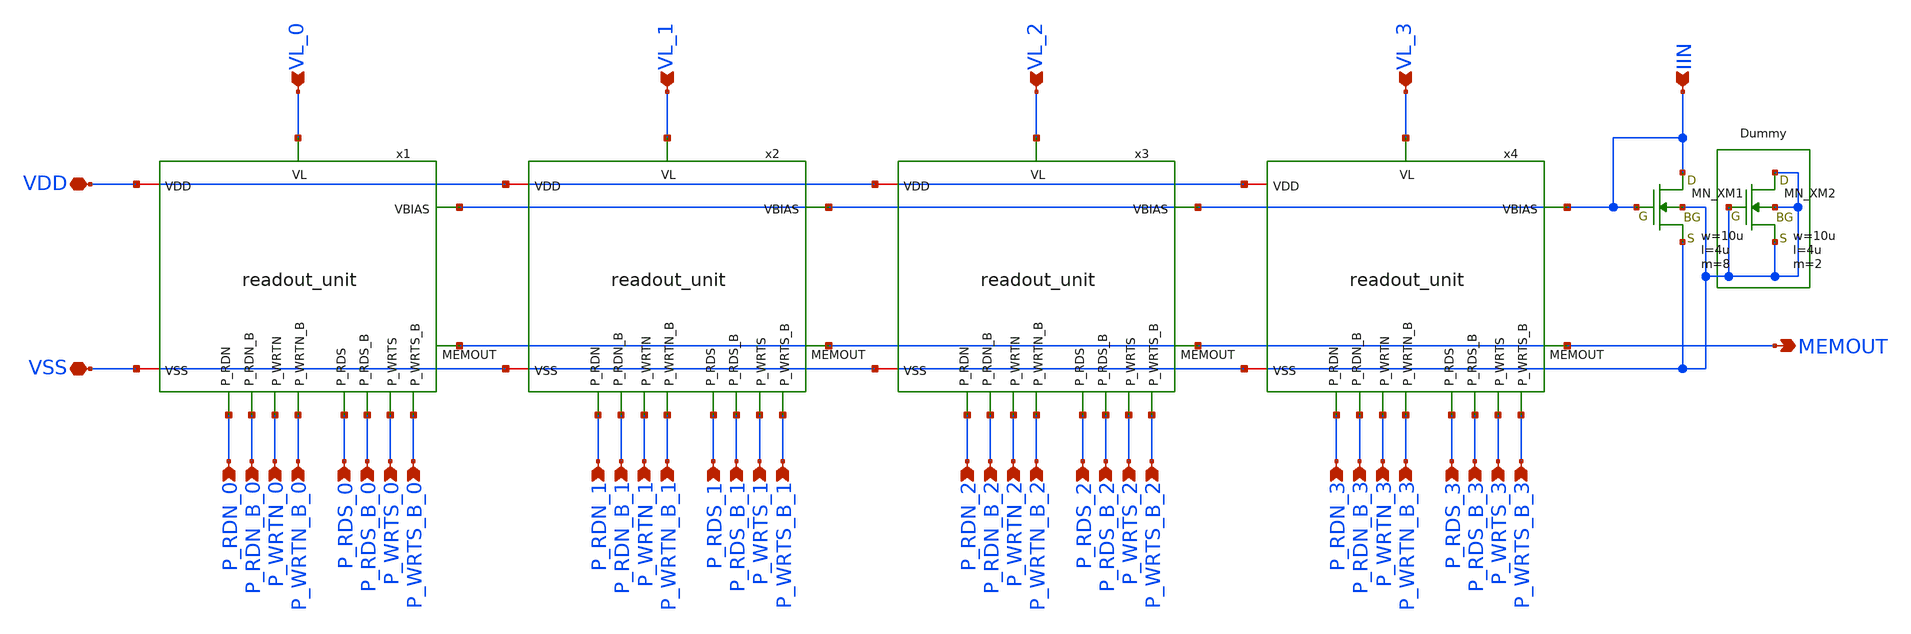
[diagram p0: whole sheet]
** sch_path: member_project/imager/YuMaehashi/design/readout.sch
**.subckt readout VL_0 VDD VSS IIN MEMOUT P_RDN_0 P_RDN_B_0 P_WRTN_0 P_WRTN_B_0 P_RDS_0 P_RDS_B_0
*+ P_WRTS_0 P_WRTS_B_0 VL_1 VL_2 VL_3 P_RDN_1 P_RDN_B_1 P_WRTN_1 P_WRTN_B_1 P_RDS_1 P_RDS_B_1 P_WRTS_1
*+ P_WRTS_B_1 P_RDN_2 P_RDN_B_2 P_WRTN_2 P_WRTN_B_2 P_RDS_2 P_RDS_B_2 P_WRTS_2 P_WRTS_B_2 P_RDN_3 P_RDN_B_3
*+ P_WRTN_3 P_WRTN_B_3 P_RDS_3 P_RDS_B_3 P_WRTS_3 P_WRTS_B_3
*.ipin VL_0
*.iopin VDD
*.iopin VSS
*.ipin IIN
*.opin MEMOUT
*.ipin P_RDN_0
*.ipin P_RDN_B_0
*.ipin P_WRTN_0
*.ipin P_WRTN_B_0
*.ipin P_RDS_0
*.ipin P_RDS_B_0
*.ipin P_WRTS_0
*.ipin P_WRTS_B_0
*.ipin VL_1
*.ipin VL_2
*.ipin VL_3
*.ipin P_RDN_1
*.ipin P_RDN_B_1
*.ipin P_WRTN_1
*.ipin P_WRTN_B_1
*.ipin P_RDS_1
*.ipin P_RDS_B_1
*.ipin P_WRTS_1
*.ipin P_WRTS_B_1
*.ipin P_RDN_2
*.ipin P_RDN_B_2
*.ipin P_WRTN_2
*.ipin P_WRTN_B_2
*.ipin P_RDS_2
*.ipin P_RDS_B_2
*.ipin P_WRTS_2
*.ipin P_WRTS_B_2
*.ipin P_RDN_3
*.ipin P_RDN_B_3
*.ipin P_WRTN_3
*.ipin P_WRTN_B_3
*.ipin P_RDS_3
*.ipin P_RDS_B_3
*.ipin P_WRTS_3
*.ipin P_WRTS_B_3
x1 VL_0 VDD IIN VSS P_WRTN_0 P_WRTN_B_0 P_WRTS_0 P_WRTS_B_0 MEMOUT P_RDS_B_0 P_RDS_0 P_RDN_B_0
+ P_RDN_0 readout_unit
x2 VL_1 VDD IIN VSS P_WRTN_1 P_WRTN_B_1 P_WRTS_1 P_WRTS_B_1 MEMOUT P_RDS_B_1 P_RDS_1 P_RDN_B_1
+ P_RDN_1 readout_unit
x3 VL_2 VDD IIN VSS P_WRTN_2 P_WRTN_B_2 P_WRTS_2 P_WRTS_B_2 MEMOUT P_RDS_B_2 P_RDS_2 P_RDN_B_2
+ P_RDN_2 readout_unit
x4 VL_3 VDD IIN VSS P_WRTN_3 P_WRTN_B_3 P_WRTS_3 P_WRTS_B_3 MEMOUT P_RDS_B_3 P_RDS_3 P_RDN_B_3
+ P_RDN_3 readout_unit
XXM1 IIN IIN VSS VSS NMOS w=10u l=4u nrd=0 nrs=0 m=8
XXM2 VSS VSS VSS VSS NMOS w=10u l=4u nrd=0 nrs=0 m=2
**.ends

* expanding   symbol:  2026_imager/readout_unit.sym # of pins=13
** sym_path: member_project/imager/YuMaehashi/design/readout_unit.sym
** sch_path: member_project/imager/YuMaehashi/design/readout_unit.sch
.subckt readout_unit VL VDD VBIAS VSS P_WRTN P_WRTN_B P_WRTS P_WRTS_B MEMOUT P_RDS_B P_RDS P_RDN_B
+ P_RDN
*.ipin VL
*.iopin VSS
*.ipin VBIAS
*.opin MEMOUT
*.ipin P_RDN
*.ipin P_RDN_B
*.ipin P_WRTN
*.ipin P_WRTN_B
*.ipin P_RDS
*.ipin P_RDS_B
*.ipin P_WRTS
*.ipin P_WRTS_B
*.iopin VDD
XXM1 VL VBIAS VSS VSS NMOS w=10u l=4u nrd=0 nrs=0 m=2
XXC1 MEM_N VSS VSS F_CSIO c=1.017p x=59.5u y=28.5u m=14
XXC2 MEM_S VSS VSS F_CSIO c=1.017p x=59.5u y=28.5u m=14
XXM2 MEM_S P_WRTS_B MEM_S VSS NMOS w=3.4u l=1u nrd=0 nrs=0 m=1
XXM3 MEM_S P_WRTS MEM_S VDD PMOS w=3.4u l=1u nrd=0 nrs=0 m=1
XXM4 VL P_WRTS MEM_S VSS NMOS w=6.8u l=1u nrd=0 nrs=0 m=1
XXM5 VL P_WRTS_B MEM_S VDD PMOS w=6.8u l=1u nrd=0 nrs=0 m=1
XXM6 MEM_N P_WRTN_B MEM_N VSS NMOS w=3.4u l=1u nrd=0 nrs=0 m=1
XXM7 MEM_N P_WRTN MEM_N VDD PMOS w=3.4u l=1u nrd=0 nrs=0 m=1
XXM8 VL P_WRTN MEM_N VSS NMOS w=6.8u l=1u nrd=0 nrs=0 m=1
XXM9 VL P_WRTN_B MEM_N VDD PMOS w=6.8u l=1u nrd=0 nrs=0 m=1
XXM10 MEM_S P_RDS_B MEM_S VSS NMOS w=3.4u l=1u nrd=0 nrs=0 m=1
XXM11 MEM_S P_RDS MEM_S VDD PMOS w=3.4u l=1u nrd=0 nrs=0 m=1
XXM12 MEM_N P_RDN_B MEM_N VSS NMOS w=3.4u l=1u nrd=0 nrs=0 m=1
XXM13 MEM_N P_RDN MEM_N VDD PMOS w=3.4u l=1u nrd=0 nrs=0 m=1
XXM14 MEM_S P_RDS MEMOUT VSS NMOS w=6.8u l=1u nrd=0 nrs=0 m=1
XXM15 MEM_S P_RDS_B MEMOUT VDD PMOS w=6.8u l=1u nrd=0 nrs=0 m=1
XXM16 MEM_N P_RDN MEMOUT VSS NMOS w=6.8u l=1u nrd=0 nrs=0 m=1
XXM17 MEM_N P_RDN_B MEMOUT VDD PMOS w=6.8u l=1u nrd=0 nrs=0 m=1
XXM18 MEMOUT P_RDS_B MEMOUT VSS NMOS w=3.4u l=1u nrd=0 nrs=0 m=1
XXM19 MEMOUT P_RDS MEMOUT VDD PMOS w=3.4u l=1u nrd=0 nrs=0 m=1
XXM20 MEMOUT P_RDN_B MEMOUT VSS NMOS w=3.4u l=1u nrd=0 nrs=0 m=1
XXM21 MEMOUT P_RDN MEMOUT VDD PMOS w=3.4u l=1u nrd=0 nrs=0 m=1
.ends

.end
